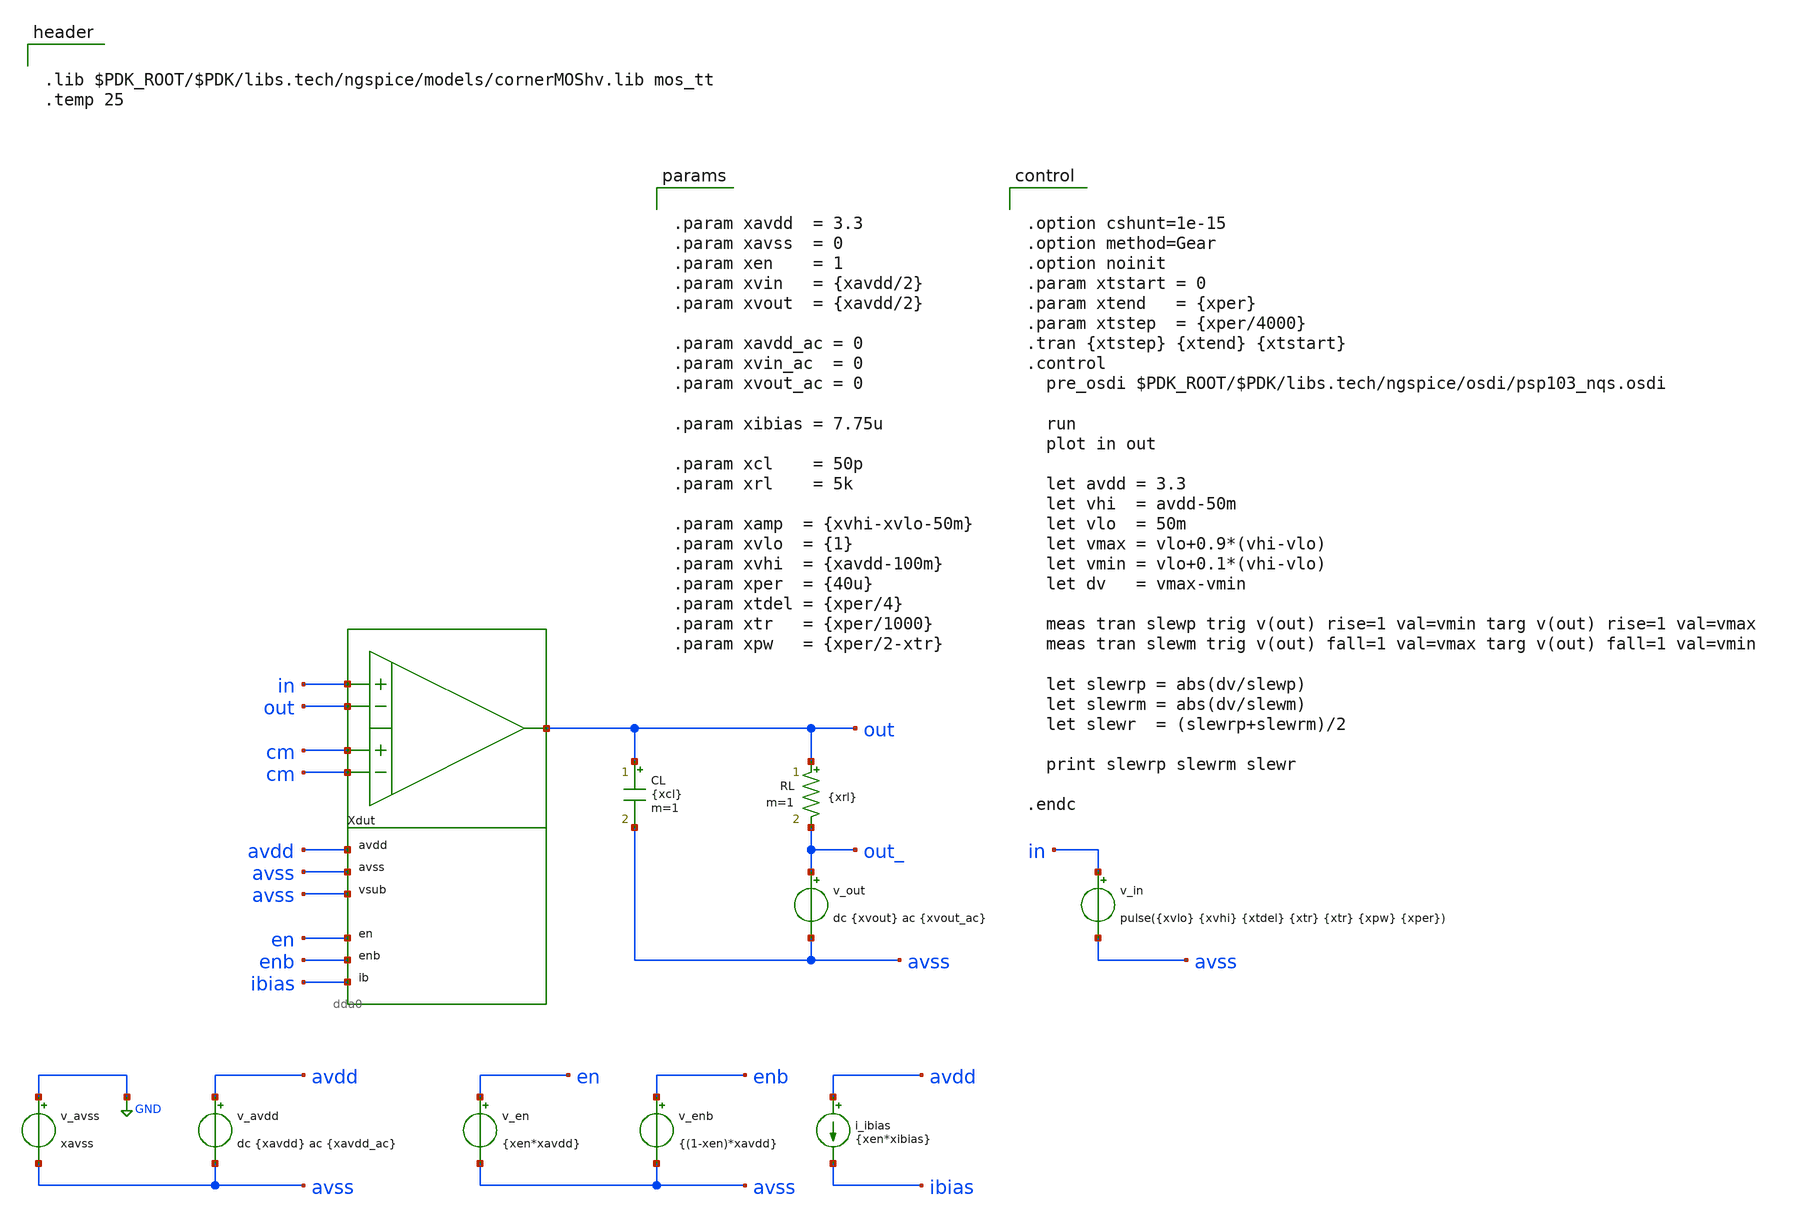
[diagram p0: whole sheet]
** sch_path: xschem/tb_dda0_buf_tran_step_large.sch
**.subckt tb_dda0_buf_tran_step_large
Xdut in out cm cm out avdd avss avss en enb ibias dda0
v_avss GND avss xavss
v_avdd avdd avss dc {xavdd} ac {xavdd_ac}
v_in in avss pulse({xvlo} {xvhi} {xtdel} {xtr} {xtr} {xpw} {xper})
v_en en avss {xen*xavdd}
v_enb enb avss {(1-xen)*xavdd}
i_ibias avdd ibias {xen*xibias}
CL out avss {xcl} m=1
v_out out_ avss dc {xvout} ac {xvout_ac}
RL out out_ {xrl} m=1
**** begin user architecture code


.lib $PDK_ROOT/$PDK/libs.tech/ngspice/models/cornerMOShv.lib mos_tt
.temp 25




.option cshunt=1e-15
.option method=Gear
.option noinit
.param xtstart = 0
.param xtend   = {xper}
.param xtstep  = {xper/4000}
.tran {xtstep} {xtend} {xtstart}
.control
  pre_osdi $PDK_ROOT/$PDK/libs.tech/ngspice/osdi/psp103_nqs.osdi

  run
  plot in out

  let avdd = 3.3
  let vhi  = avdd-50m
  let vlo  = 50m
  let vmax = vlo+0.9*(vhi-vlo)
  let vmin = vlo+0.1*(vhi-vlo)
  let dv   = vmax-vmin

  meas tran slewp trig v(out) rise=1 val=vmin targ v(out) rise=1 val=vmax
  meas tran slewm trig v(out) fall=1 val=vmax targ v(out) fall=1 val=vmin

  let slewrp = abs(dv/slewp)
  let slewrm = abs(dv/slewm)
  let slewr  = (slewrp+slewrm)/2

  print slewrp slewrm slewr

.endc




.param xavdd  = 3.3
.param xavss  = 0
.param xen    = 1
.param xvin   = {xavdd/2}
.param xvout  = {xavdd/2}

.param xavdd_ac = 0
.param xvin_ac  = 0
.param xvout_ac = 0

.param xibias = 7.75u

.param xcl    = 50p
.param xrl    = 5k

.param xamp  = {xvhi-xvlo-50m}
.param xvlo  = {1}
.param xvhi  = {xavdd-100m}
.param xper  = {40u}
.param xtdel = {xper/4}
.param xtr   = {xper/1000}
.param xpw   = {xper/2-xtr}


**** end user architecture code
**.ends
.GLOBAL GND
.end
